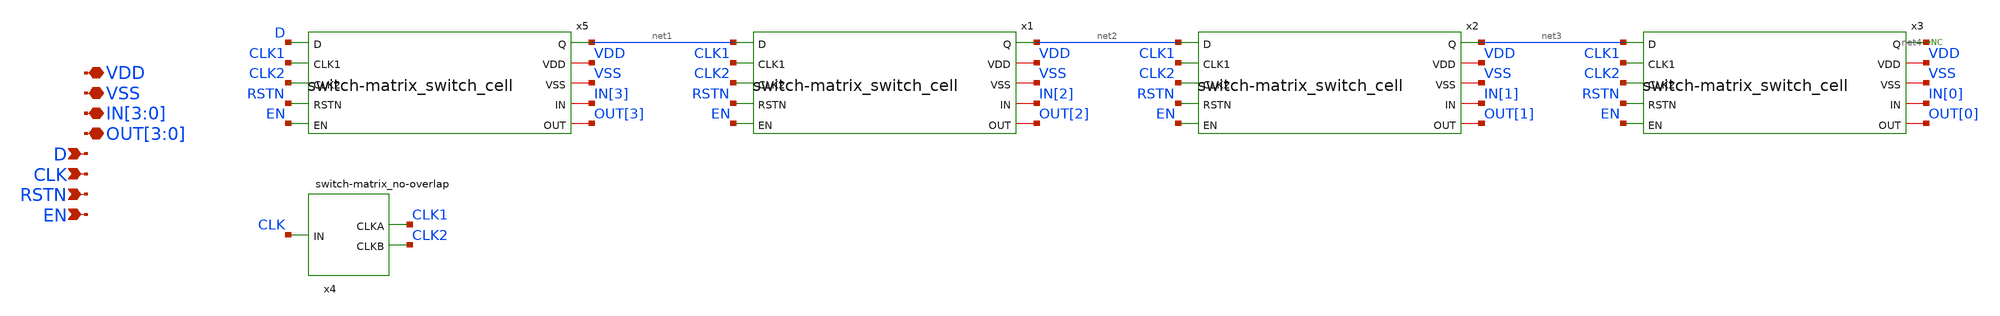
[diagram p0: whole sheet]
** sch_path: designs/libs/core_analog/switch-matrix/switch-matrix_tg_array_4x1.sch
**.subckt switch-matrix_tg_array_4x1 VDD VSS IN[3],IN[2],IN[1],IN[0] OUT[3],OUT[2],OUT[1],OUT[0] D
*+ RSTN CLK EN
*.iopin VDD
*.iopin VSS
*.iopin IN[3],IN[2],IN[1],IN[0]
*.iopin OUT[3],OUT[2],OUT[1],OUT[0]
*.ipin D
*.ipin RSTN
*.ipin CLK
*.ipin EN
* noconn #net4
x5 net1 VDD VSS D CLK1 CLK2 RSTN EN IN[3] OUT[3] switch-matrix_switch_cell
x1 net2 VDD VSS net1 CLK1 CLK2 RSTN EN IN[2] OUT[2] switch-matrix_switch_cell
x2 net3 VDD VSS net2 CLK1 CLK2 RSTN EN IN[1] OUT[1] switch-matrix_switch_cell
x3 net4 VDD VSS net3 CLK1 CLK2 RSTN EN IN[0] OUT[0] switch-matrix_switch_cell
x4 CLK VSS VDD CLK1 CLK2 switch-matrix_no-overlap
**.ends
.end
